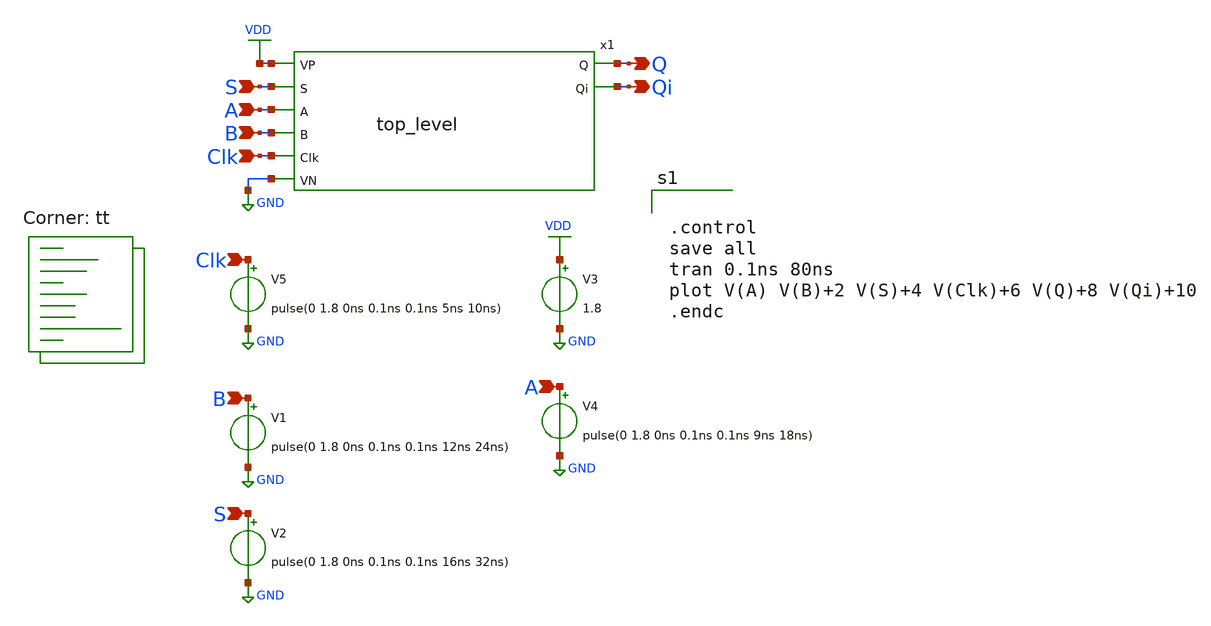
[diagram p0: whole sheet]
** sch_path: top_level/xschem/tb_xschem_top_level.sch
**.subckt tb_xschem_top_level A B A B Q S S Qi Clk Clk
*.ipin A
*.ipin B
*.ipin A
*.ipin B
*.opin Q
*.ipin S
*.ipin S
*.opin Qi
*.ipin Clk
*.ipin Clk
V3 VDD GND 1.8
V4 A GND pulse(0 1.8 0ns 0.1ns 0.1ns 9ns 18ns)
V1 B GND pulse(0 1.8 0ns 0.1ns 0.1ns 12ns 24ns)
V2 S GND pulse(0 1.8 0ns 0.1ns 0.1ns 16ns 32ns)
x1 VDD Q S Qi A B Clk GND top_level
V5 Clk GND pulse(0 1.8 0ns 0.1ns 0.1ns 5ns 10ns)
**** begin user architecture code
.lib $::SKYWATER_MODELS/sky130.lib.spice tt


.control
save all
tran 0.1ns 80ns
plot V(A) V(B)+2 V(S)+4 V(Clk)+6 V(Q)+8 V(Qi)+10
.endc


**** end user architecture code
**.ends

* expanding   symbol:  top_level.sym # of pins=8
** sym_path: top_level/xschem/top_level.sym
** sch_path: top_level/xschem/top_level.sch
.subckt top_level VP Q S Qi A B Clk VN
*.ipin VP
*.ipin S
*.ipin A
*.ipin B
*.ipin Clk
*.ipin VN
*.opin Q
*.opin Qi
x1 Q VP net1 Clk VN Qi dff
x2 VP net1 S VN A B mux
.ends


* expanding   symbol:  /foss/designs/APIC_Mux_DFF/dff/xschem/dff.sym # of pins=6
** sym_path: dff/xschem/dff.sym
** sch_path: dff/xschem/dff.sch
.subckt dff Q VP D Clk VN Qi
*.ipin D
*.ipin Clk
*.ipin VP
*.ipin VN
*.opin Q
*.opin Qi
x1 VP D net1 VN inverter
x2 VP net2 Clk D VN nand
x3 VP net3 Clk net1 VN nand
x4 VP Qi net3 Q VN nand
x5 VP Q Qi net2 VN nand
.ends


* expanding   symbol:  /foss/designs/APIC_Mux_DFF/mux/xschem/mux.sym # of pins=6
** sym_path: mux/xschem/mux.sym
** sch_path: mux/xschem/mux.sch
.subckt mux VP D S VN A B
*.ipin S
*.ipin A
*.ipin B
*.opin D
*.ipin VP
*.ipin VN
x1 VP S net1 VN inverter
x0 VP net2 A net1 VN and
x2 VP net2 S B VN and
x3 VP D net2 net2 VN or
.ends


* expanding   symbol:  /foss/designs/APIC_Mux_DFF/basic_cell/single_cell/inverter/inverter.sym # of
*+ pins=4
** sym_path: basic_cell/single_cell/inverter/inverter.sym
** sch_path: basic_cell/single_cell/inverter/inverter.sch
.subckt inverter VP A OUT VN
*.ipin A
*.ipin VP
*.ipin VN
*.opin OUT
XM1 OUT A VP VP sky130_fd_pr__pfet_01v8 L=0.15 W=3 nf=1 ad='int((nf+1)/2) * W/nf * 0.29' as='int((nf+2)/2) * W/nf * 0.29'
+ pd='2*int((nf+1)/2) * (W/nf + 0.29)' ps='2*int((nf+2)/2) * (W/nf + 0.29)' nrd='0.29 / W' nrs='0.29 / W'
+ sa=0 sb=0 sd=0 mult=1 m=1
XM2 OUT A VN VN sky130_fd_pr__nfet_01v8 L=0.15 W=1 nf=1 ad='int((nf+1)/2) * W/nf * 0.29' as='int((nf+2)/2) * W/nf * 0.29'
+ pd='2*int((nf+1)/2) * (W/nf + 0.29)' ps='2*int((nf+2)/2) * (W/nf + 0.29)' nrd='0.29 / W' nrs='0.29 / W'
+ sa=0 sb=0 sd=0 mult=1 m=1
.ends


* expanding   symbol:  /foss/designs/APIC_Mux_DFF/basic_cell/single_cell/nand/nand.sym # of pins=5
** sym_path: basic_cell/single_cell/nand/nand.sym
** sch_path: basic_cell/single_cell/nand/nand.sch
.subckt nand VP OUT B A VN
*.opin OUT
*.ipin A
*.ipin B
*.ipin VN
*.ipin VP
XM4 OUT A net1 VN sky130_fd_pr__nfet_01v8 L=0.15 W=1 nf=1 ad='int((nf+1)/2) * W/nf * 0.29' as='int((nf+2)/2) * W/nf * 0.29'
+ pd='2*int((nf+1)/2) * (W/nf + 0.29)' ps='2*int((nf+2)/2) * (W/nf + 0.29)' nrd='0.29 / W' nrs='0.29 / W'
+ sa=0 sb=0 sd=0 mult=1 m=1
XM3 net1 B VN VN sky130_fd_pr__nfet_01v8 L=0.15 W=1 nf=1 ad='int((nf+1)/2) * W/nf * 0.29' as='int((nf+2)/2) * W/nf * 0.29'
+ pd='2*int((nf+1)/2) * (W/nf + 0.29)' ps='2*int((nf+2)/2) * (W/nf + 0.29)' nrd='0.29 / W' nrs='0.29 / W'
+ sa=0 sb=0 sd=0 mult=1 m=1
XM1 OUT A VP VP sky130_fd_pr__pfet_01v8 L=0.15 W=3 nf=1 ad='int((nf+1)/2) * W/nf * 0.29' as='int((nf+2)/2) * W/nf * 0.29'
+ pd='2*int((nf+1)/2) * (W/nf + 0.29)' ps='2*int((nf+2)/2) * (W/nf + 0.29)' nrd='0.29 / W' nrs='0.29 / W'
+ sa=0 sb=0 sd=0 mult=1 m=1
XM2 OUT B VP VP sky130_fd_pr__pfet_01v8 L=0.15 W=3 nf=1 ad='int((nf+1)/2) * W/nf * 0.29' as='int((nf+2)/2) * W/nf * 0.29'
+ pd='2*int((nf+1)/2) * (W/nf + 0.29)' ps='2*int((nf+2)/2) * (W/nf + 0.29)' nrd='0.29 / W' nrs='0.29 / W'
+ sa=0 sb=0 sd=0 mult=1 m=1
.ends


* expanding   symbol:  /foss/designs/APIC_Mux_DFF/basic_cell/and/xschem/and.sym # of pins=5
** sym_path: basic_cell/and/xschem/and.sym
** sch_path: basic_cell/and/xschem/and.sch
.subckt and VP OUT B A VN
*.ipin VP
*.ipin B
*.ipin A
*.ipin VN
*.opin OUT
x1 VP net1 B A VN nand
x2 VP net1 OUT VN inverter
.ends


* expanding   symbol:  /foss/designs/APIC_Mux_DFF/basic_cell/or/xschem/or.sym # of pins=5
** sym_path: basic_cell/or/xschem/or.sym
** sch_path: basic_cell/or/xschem/or.sch
.subckt or VP OUT A B VN
*.ipin VP
*.ipin A
*.ipin B
*.ipin VN
*.opin OUT
x1 VP A B net1 VN nor
x2 VP net1 OUT VN inverter
.ends


* expanding   symbol:  /foss/designs/APIC_Mux_DFF/basic_cell/single_cell/nor/nor.sym # of pins=5
** sym_path: basic_cell/single_cell/nor/nor.sym
** sch_path: basic_cell/single_cell/nor/nor.sch
.subckt nor VP A B OUT VN
*.ipin A
*.ipin B
*.ipin VP
*.ipin VN
*.opin OUT
XM1 OUT A VN VN sky130_fd_pr__nfet_01v8 L=0.15 W=1 nf=1 ad='int((nf+1)/2) * W/nf * 0.29' as='int((nf+2)/2) * W/nf * 0.29'
+ pd='2*int((nf+1)/2) * (W/nf + 0.29)' ps='2*int((nf+2)/2) * (W/nf + 0.29)' nrd='0.29 / W' nrs='0.29 / W'
+ sa=0 sb=0 sd=0 mult=1 m=1
XM2 OUT B VN VN sky130_fd_pr__nfet_01v8 L=0.15 W=1 nf=1 ad='int((nf+1)/2) * W/nf * 0.29' as='int((nf+2)/2) * W/nf * 0.29'
+ pd='2*int((nf+1)/2) * (W/nf + 0.29)' ps='2*int((nf+2)/2) * (W/nf + 0.29)' nrd='0.29 / W' nrs='0.29 / W'
+ sa=0 sb=0 sd=0 mult=1 m=1
XM3 OUT B net1 VP sky130_fd_pr__pfet_01v8 L=0.15 W=3 nf=1 ad='int((nf+1)/2) * W/nf * 0.29' as='int((nf+2)/2) * W/nf * 0.29'
+ pd='2*int((nf+1)/2) * (W/nf + 0.29)' ps='2*int((nf+2)/2) * (W/nf + 0.29)' nrd='0.29 / W' nrs='0.29 / W'
+ sa=0 sb=0 sd=0 mult=1 m=1
XM4 net1 A VP VP sky130_fd_pr__pfet_01v8 L=0.15 W=3 nf=1 ad='int((nf+1)/2) * W/nf * 0.29' as='int((nf+2)/2) * W/nf * 0.29'
+ pd='2*int((nf+1)/2) * (W/nf + 0.29)' ps='2*int((nf+2)/2) * (W/nf + 0.29)' nrd='0.29 / W' nrs='0.29 / W'
+ sa=0 sb=0 sd=0 mult=1 m=1
.ends

.GLOBAL VDD
.GLOBAL GND
.end
